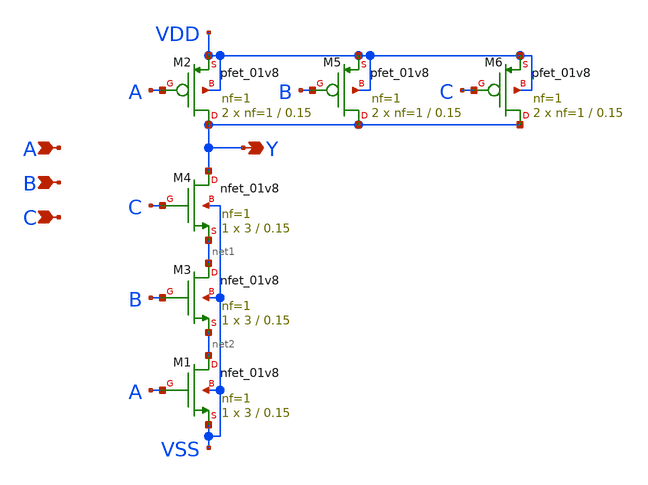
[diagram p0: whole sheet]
** sch_path: lib/xschem/NAND3X1.sch
**.subckt NAND3X1 Y A B C
*.opin Y
*.ipin A
*.ipin B
*.ipin C
XM1 net2 A VSS VSS sky130_fd_pr__nfet_01v8 L=0.15 W=3 nf=1 ad='int((nf+1)/2) * W/nf * 0.29' as='int((nf+2)/2) * W/nf * 0.29'
+ pd='2*int((nf+1)/2) * (W/nf + 0.29)' ps='2*int((nf+2)/2) * (W/nf + 0.29)' nrd='0.29 / W' nrs='0.29 / W'
+ sa=0 sb=0 sd=0 mult=1 m=1
XM2 Y A VDD VDD sky130_fd_pr__pfet_01v8 L=0.15 W=nf=1 nf=1 ad='int((nf+1)/2) * W/nf * 0.29' as='int((nf+2)/2) * W/nf * 0.29'
+ pd='2*int((nf+1)/2) * (W/nf + 0.29)' ps='2*int((nf+2)/2) * (W/nf + 0.29)' nrd='0.29 / W' nrs='0.29 / W'
+ sa=0 sb=0 sd=0 mult=2 m=2
XM3 net1 B net2 VSS sky130_fd_pr__nfet_01v8 L=0.15 W=3 nf=1 ad='int((nf+1)/2) * W/nf * 0.29' as='int((nf+2)/2) * W/nf * 0.29'
+ pd='2*int((nf+1)/2) * (W/nf + 0.29)' ps='2*int((nf+2)/2) * (W/nf + 0.29)' nrd='0.29 / W' nrs='0.29 / W'
+ sa=0 sb=0 sd=0 mult=1 m=1
XM4 Y C net1 VSS sky130_fd_pr__nfet_01v8 L=0.15 W=3 nf=1 ad='int((nf+1)/2) * W/nf * 0.29' as='int((nf+2)/2) * W/nf * 0.29'
+ pd='2*int((nf+1)/2) * (W/nf + 0.29)' ps='2*int((nf+2)/2) * (W/nf + 0.29)' nrd='0.29 / W' nrs='0.29 / W'
+ sa=0 sb=0 sd=0 mult=1 m=1
XM5 Y B VDD VDD sky130_fd_pr__pfet_01v8 L=0.15 W=nf=1 nf=1 ad='int((nf+1)/2) * W/nf * 0.29' as='int((nf+2)/2) * W/nf * 0.29'
+ pd='2*int((nf+1)/2) * (W/nf + 0.29)' ps='2*int((nf+2)/2) * (W/nf + 0.29)' nrd='0.29 / W' nrs='0.29 / W'
+ sa=0 sb=0 sd=0 mult=2 m=2
XM6 Y C VDD VDD sky130_fd_pr__pfet_01v8 L=0.15 W=nf=1 nf=1 ad='int((nf+1)/2) * W/nf * 0.29' as='int((nf+2)/2) * W/nf * 0.29'
+ pd='2*int((nf+1)/2) * (W/nf + 0.29)' ps='2*int((nf+2)/2) * (W/nf + 0.29)' nrd='0.29 / W' nrs='0.29 / W'
+ sa=0 sb=0 sd=0 mult=2 m=2
**.ends
.end
